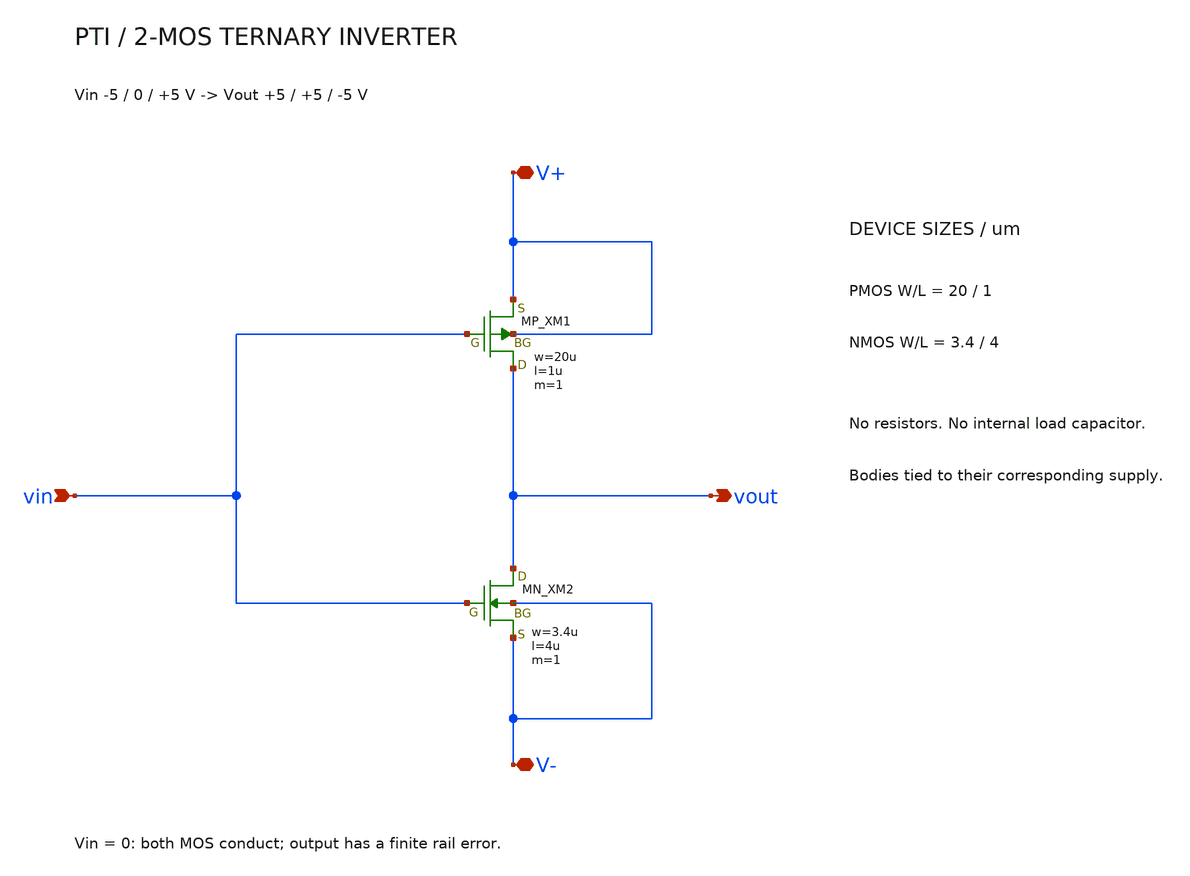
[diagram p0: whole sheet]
** sch_path: member_project/balanced-ternary-logic/PenguinEino/pti.sch
**.subckt pti V+ vout vin V-
*.iopin V+
*.opin vout
*.ipin vin
*.iopin V-
XXM1 vout vin V+ V+ PMOS w=20u l=1u nrd=0 nrs=0 m=1
XXM2 vout vin V- V- NMOS w=3.4u l=4u nrd=0 nrs=0 m=1
**.ends
.end
